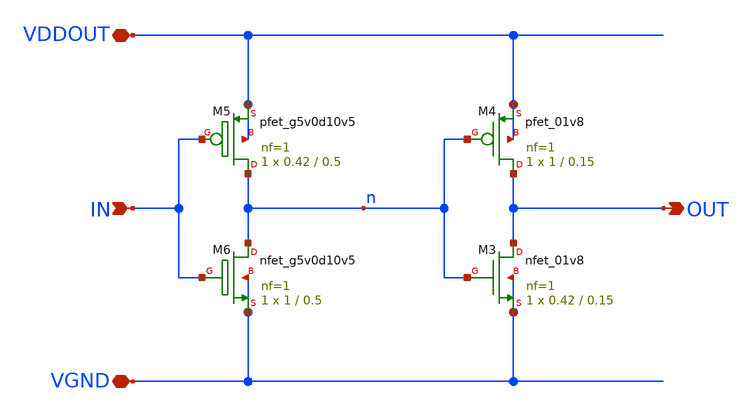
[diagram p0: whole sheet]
** sch_path: tt_um_tt08_aicd_playground/dependencies/sky130_leo_ip__levelshifter/xschem/sky130_leo_ip__levelshifter_down.sch
**.subckt sky130_leo_ip__levelshifter_down IN VGND OUT VDDOUT
*.ipin IN
*.iopin VGND
*.opin OUT
*.iopin VDDOUT
XM3 OUT n VGND VGND sky130_fd_pr__nfet_01v8 L=0.15 W=0.42 nf=1 ad='int((nf+1)/2) * W/nf * 0.29' as='int((nf+2)/2) * W/nf * 0.29'
+ pd='2*int((nf+1)/2) * (W/nf + 0.29)' ps='2*int((nf+2)/2) * (W/nf + 0.29)' nrd='0.29 / W' nrs='0.29 / W'
+ sa=0 sb=0 sd=0 mult=1 m=1
XM4 OUT n VDDOUT VDDOUT sky130_fd_pr__pfet_01v8 L=0.15 W=1 nf=1 ad='int((nf+1)/2) * W/nf * 0.29' as='int((nf+2)/2) * W/nf * 0.29'
+ pd='2*int((nf+1)/2) * (W/nf + 0.29)' ps='2*int((nf+2)/2) * (W/nf + 0.29)' nrd='0.29 / W' nrs='0.29 / W'
+ sa=0 sb=0 sd=0 mult=1 m=1
XM5 n IN VDDOUT VDDOUT sky130_fd_pr__pfet_g5v0d10v5 L=0.5 W=0.42 nf=1 ad='int((nf+1)/2) * W/nf * 0.29'
+ as='int((nf+2)/2) * W/nf * 0.29' pd='2*int((nf+1)/2) * (W/nf + 0.29)' ps='2*int((nf+2)/2) * (W/nf + 0.29)'
+ nrd='0.29 / W' nrs='0.29 / W' sa=0 sb=0 sd=0 mult=1 m=1
XM6 n IN VGND VGND sky130_fd_pr__nfet_g5v0d10v5 L=0.5 W=1 nf=1 ad='int((nf+1)/2) * W/nf * 0.29' as='int((nf+2)/2) * W/nf * 0.29'
+ pd='2*int((nf+1)/2) * (W/nf + 0.29)' ps='2*int((nf+2)/2) * (W/nf + 0.29)' nrd='0.29 / W' nrs='0.29 / W'
+ sa=0 sb=0 sd=0 mult=1 m=1
**.ends
.end
